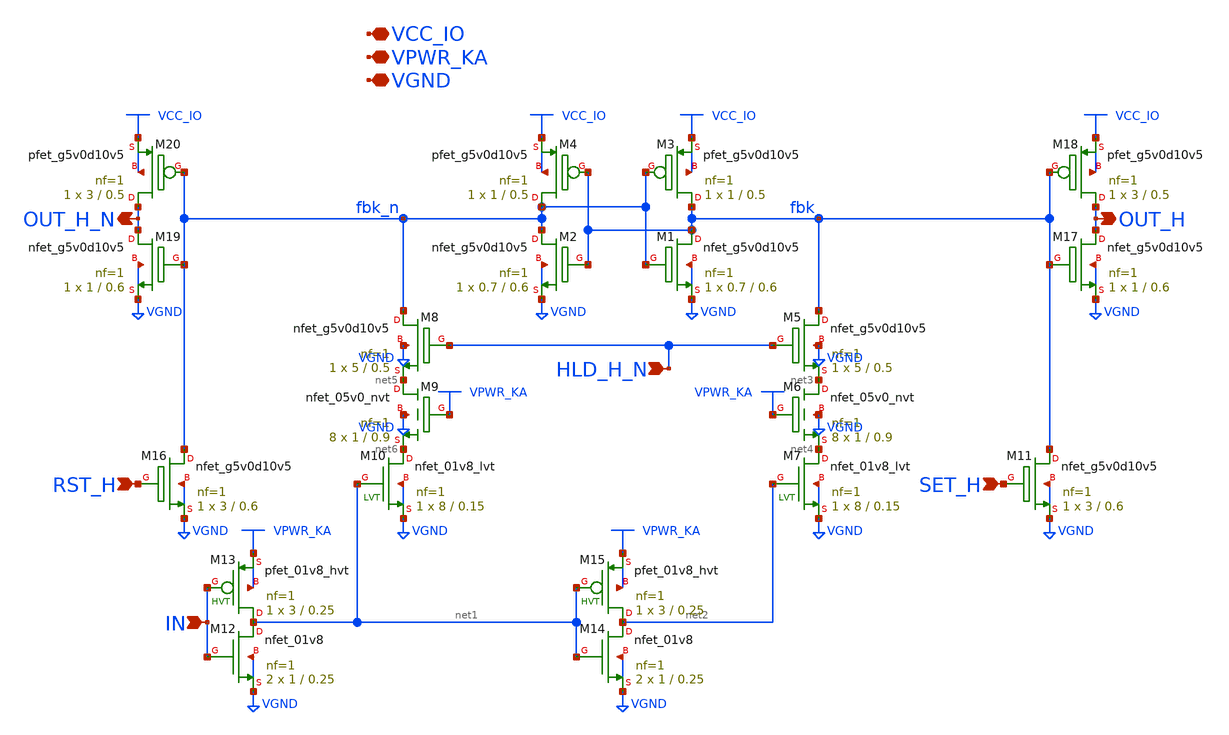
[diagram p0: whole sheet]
** sch_path: gpio_dat_ls.sch
* Copyright 2023 David Mitchell Bailey
* Licensed under the Apache License, Version 2.0 (the "License");
* you may not use this file except in compliance with the License.
* You may obtain a copy of the License at
* https://www.apache.org/licenses/LICENSE-2.0
* Unless required by applicable law or agreed to in writing, software
* distributed under the License is distributed on an "AS IS" BASIS,
* WITHOUT WARRANTIES OR CONDITIONS OF ANY KIND, either express or implied.
* See the License for the specific language governing permissions and
* limitations under the License.
**.subckt gpio_dat_ls IN HLD_H_N SET_H RST_H OUT_H_N OUT_H VCC_IO VPWR_KA VGND
*.ipin IN
*.ipin HLD_H_N
*.ipin SET_H
*.ipin RST_H
*.opin OUT_H_N
*.opin OUT_H
*.iopin VCC_IO
*.iopin VPWR_KA
*.iopin VGND
XM1 fbk fbk_n VGND VGND sky130_fd_pr__nfet_g5v0d10v5 L=0.6 W=0.7 nf=1 ad='int((nf+1)/2) * W/nf * 0.29'
+ as='int((nf+2)/2) * W/nf * 0.29' pd='2*int((nf+1)/2) * (W/nf + 0.29)' ps='2*int((nf+2)/2) * (W/nf + 0.29)'
+ nrd='0.29 / W' nrs='0.29 / W' sa=0 sb=0 sd=0 mult=1 m=1
XM2 fbk_n fbk VGND VGND sky130_fd_pr__nfet_g5v0d10v5 L=0.6 W=0.7 nf=1 ad='int((nf+1)/2) * W/nf * 0.29'
+ as='int((nf+2)/2) * W/nf * 0.29' pd='2*int((nf+1)/2) * (W/nf + 0.29)' ps='2*int((nf+2)/2) * (W/nf + 0.29)'
+ nrd='0.29 / W' nrs='0.29 / W' sa=0 sb=0 sd=0 mult=1 m=1
XM3 fbk fbk_n VCC_IO VCC_IO sky130_fd_pr__pfet_g5v0d10v5 L=0.5 W=1 nf=1 ad='int((nf+1)/2) * W/nf * 0.29'
+ as='int((nf+2)/2) * W/nf * 0.29' pd='2*int((nf+1)/2) * (W/nf + 0.29)' ps='2*int((nf+2)/2) * (W/nf + 0.29)'
+ nrd='0.29 / W' nrs='0.29 / W' sa=0 sb=0 sd=0 mult=1 m=1
XM4 fbk_n fbk VCC_IO VCC_IO sky130_fd_pr__pfet_g5v0d10v5 L=0.5 W=1 nf=1 ad='int((nf+1)/2) * W/nf * 0.29'
+ as='int((nf+2)/2) * W/nf * 0.29' pd='2*int((nf+1)/2) * (W/nf + 0.29)' ps='2*int((nf+2)/2) * (W/nf + 0.29)'
+ nrd='0.29 / W' nrs='0.29 / W' sa=0 sb=0 sd=0 mult=1 m=1
XM5 fbk HLD_H_N net3 VGND sky130_fd_pr__nfet_g5v0d10v5 L=0.5 W=5 nf=1 ad='int((nf+1)/2) * W/nf * 0.29'
+ as='int((nf+2)/2) * W/nf * 0.29' pd='2*int((nf+1)/2) * (W/nf + 0.29)' ps='2*int((nf+2)/2) * (W/nf + 0.29)'
+ nrd='0.29 / W' nrs='0.29 / W' sa=0 sb=0 sd=0 mult=1 m=1
XM6 net3 VPWR_KA net4 VGND sky130_fd_pr__nfet_05v0_nvt L=0.9 W=1 nf=1 ad='int((nf+1)/2) * W/nf * 0.29'
+ as='int((nf+2)/2) * W/nf * 0.29' pd='2*int((nf+1)/2) * (W/nf + 0.29)' ps='2*int((nf+2)/2) * (W/nf + 0.29)'
+ nrd='0.29 / W' nrs='0.29 / W' sa=0 sb=0 sd=0 mult=8 m=8
XM7 net4 net2 VGND VGND sky130_fd_pr__nfet_01v8_lvt L=0.15 W=8 nf=1 ad='int((nf+1)/2) * W/nf * 0.29'
+ as='int((nf+2)/2) * W/nf * 0.29' pd='2*int((nf+1)/2) * (W/nf + 0.29)' ps='2*int((nf+2)/2) * (W/nf + 0.29)'
+ nrd='0.29 / W' nrs='0.29 / W' sa=0 sb=0 sd=0 mult=1 m=1
XM8 fbk_n HLD_H_N net5 VGND sky130_fd_pr__nfet_g5v0d10v5 L=0.5 W=5 nf=1 ad='int((nf+1)/2) * W/nf * 0.29'
+ as='int((nf+2)/2) * W/nf * 0.29' pd='2*int((nf+1)/2) * (W/nf + 0.29)' ps='2*int((nf+2)/2) * (W/nf + 0.29)'
+ nrd='0.29 / W' nrs='0.29 / W' sa=0 sb=0 sd=0 mult=1 m=1
XM9 net5 VPWR_KA net6 VGND sky130_fd_pr__nfet_05v0_nvt L=0.9 W=1 nf=1 ad='int((nf+1)/2) * W/nf * 0.29'
+ as='int((nf+2)/2) * W/nf * 0.29' pd='2*int((nf+1)/2) * (W/nf + 0.29)' ps='2*int((nf+2)/2) * (W/nf + 0.29)'
+ nrd='0.29 / W' nrs='0.29 / W' sa=0 sb=0 sd=0 mult=8 m=8
XM10 net6 net1 VGND VGND sky130_fd_pr__nfet_01v8_lvt L=0.15 W=8 nf=1 ad='int((nf+1)/2) * W/nf * 0.29'
+ as='int((nf+2)/2) * W/nf * 0.29' pd='2*int((nf+1)/2) * (W/nf + 0.29)' ps='2*int((nf+2)/2) * (W/nf + 0.29)'
+ nrd='0.29 / W' nrs='0.29 / W' sa=0 sb=0 sd=0 mult=1 m=1
XM11 fbk SET_H VGND VGND sky130_fd_pr__nfet_g5v0d10v5 L=0.6 W=3 nf=1 ad='int((nf+1)/2) * W/nf * 0.29'
+ as='int((nf+2)/2) * W/nf * 0.29' pd='2*int((nf+1)/2) * (W/nf + 0.29)' ps='2*int((nf+2)/2) * (W/nf + 0.29)'
+ nrd='0.29 / W' nrs='0.29 / W' sa=0 sb=0 sd=0 mult=1 m=1
XM12 net1 IN VGND VGND sky130_fd_pr__nfet_01v8 L=0.25 W=1 nf=1 ad='int((nf+1)/2) * W/nf * 0.29' as='int((nf+2)/2) * W/nf * 0.29'
+ pd='2*int((nf+1)/2) * (W/nf + 0.29)' ps='2*int((nf+2)/2) * (W/nf + 0.29)' nrd='0.29 / W' nrs='0.29 / W'
+ sa=0 sb=0 sd=0 mult=2 m=2
XM14 net2 net1 VGND VGND sky130_fd_pr__nfet_01v8 L=0.25 W=1 nf=1 ad='int((nf+1)/2) * W/nf * 0.29' as='int((nf+2)/2) * W/nf * 0.29'
+ pd='2*int((nf+1)/2) * (W/nf + 0.29)' ps='2*int((nf+2)/2) * (W/nf + 0.29)' nrd='0.29 / W' nrs='0.29 / W'
+ sa=0 sb=0 sd=0 mult=2 m=2
XM16 fbk_n RST_H VGND VGND sky130_fd_pr__nfet_g5v0d10v5 L=0.6 W=3 nf=1 ad='int((nf+1)/2) * W/nf * 0.29'
+ as='int((nf+2)/2) * W/nf * 0.29' pd='2*int((nf+1)/2) * (W/nf + 0.29)' ps='2*int((nf+2)/2) * (W/nf + 0.29)'
+ nrd='0.29 / W' nrs='0.29 / W' sa=0 sb=0 sd=0 mult=1 m=1
XM17 OUT_H fbk VGND VGND sky130_fd_pr__nfet_g5v0d10v5 L=0.6 W=1 nf=1 ad='int((nf+1)/2) * W/nf * 0.29'
+ as='int((nf+2)/2) * W/nf * 0.29' pd='2*int((nf+1)/2) * (W/nf + 0.29)' ps='2*int((nf+2)/2) * (W/nf + 0.29)'
+ nrd='0.29 / W' nrs='0.29 / W' sa=0 sb=0 sd=0 mult=1 m=1
XM18 OUT_H fbk VCC_IO VCC_IO sky130_fd_pr__pfet_g5v0d10v5 L=0.5 W=3 nf=1 ad='int((nf+1)/2) * W/nf * 0.29'
+ as='int((nf+2)/2) * W/nf * 0.29' pd='2*int((nf+1)/2) * (W/nf + 0.29)' ps='2*int((nf+2)/2) * (W/nf + 0.29)'
+ nrd='0.29 / W' nrs='0.29 / W' sa=0 sb=0 sd=0 mult=1 m=1
XM19 OUT_H_N fbk_n VGND VGND sky130_fd_pr__nfet_g5v0d10v5 L=0.6 W=1 nf=1 ad='int((nf+1)/2) * W/nf * 0.29'
+ as='int((nf+2)/2) * W/nf * 0.29' pd='2*int((nf+1)/2) * (W/nf + 0.29)' ps='2*int((nf+2)/2) * (W/nf + 0.29)'
+ nrd='0.29 / W' nrs='0.29 / W' sa=0 sb=0 sd=0 mult=1 m=1
XM20 OUT_H_N fbk_n VCC_IO VCC_IO sky130_fd_pr__pfet_g5v0d10v5 L=0.5 W=3 nf=1 ad='int((nf+1)/2) * W/nf * 0.29'
+ as='int((nf+2)/2) * W/nf * 0.29' pd='2*int((nf+1)/2) * (W/nf + 0.29)' ps='2*int((nf+2)/2) * (W/nf + 0.29)'
+ nrd='0.29 / W' nrs='0.29 / W' sa=0 sb=0 sd=0 mult=1 m=1
XM13 net1 IN VPWR_KA VPWR_KA sky130_fd_pr__pfet_01v8_hvt L=0.25 W=3 nf=1 ad='int((nf+1)/2) * W/nf * 0.29'
+ as='int((nf+2)/2) * W/nf * 0.29' pd='2*int((nf+1)/2) * (W/nf + 0.29)' ps='2*int((nf+2)/2) * (W/nf + 0.29)'
+ nrd='0.29 / W' nrs='0.29 / W' sa=0 sb=0 sd=0 mult=1 m=1
XM15 net2 net1 VPWR_KA VPWR_KA sky130_fd_pr__pfet_01v8_hvt L=0.25 W=3 nf=1 ad='int((nf+1)/2) * W/nf * 0.29'
+ as='int((nf+2)/2) * W/nf * 0.29' pd='2*int((nf+1)/2) * (W/nf + 0.29)' ps='2*int((nf+2)/2) * (W/nf + 0.29)'
+ nrd='0.29 / W' nrs='0.29 / W' sa=0 sb=0 sd=0 mult=1 m=1
**.ends
.end
